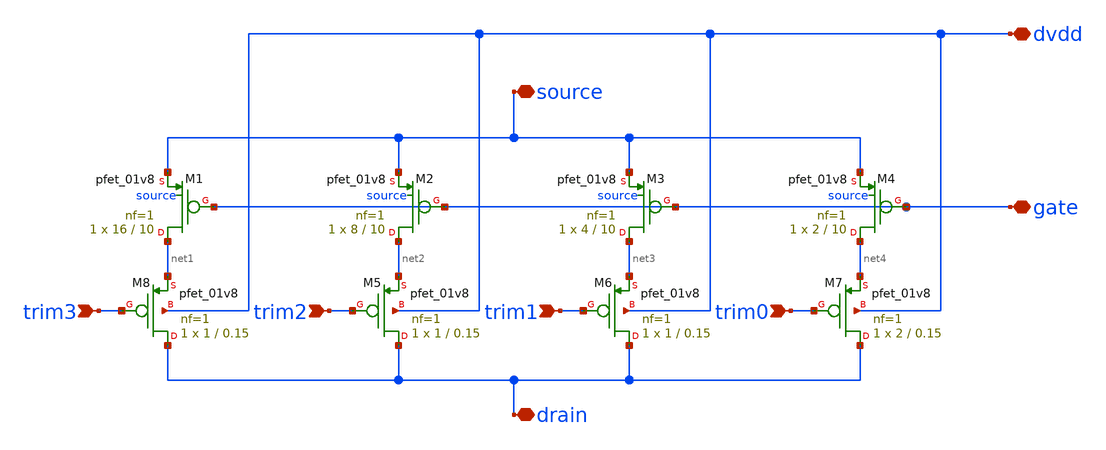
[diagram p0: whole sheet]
** sch_path: xschem/trim_pfet.sch
**.subckt trim_pfet trim0 trim1 trim2 trim3 dvdd drain source gate
*.ipin trim0
*.ipin trim1
*.ipin trim2
*.ipin trim3
*.iopin dvdd
*.iopin drain
*.iopin source
*.iopin gate
XM4 net4 gate source source sky130_fd_pr__pfet_01v8 L=10 W=2 nf=1 ad='int((nf+1)/2) * W/nf * 0.29' as='int((nf+2)/2) * W/nf * 0.29'
+ pd='2*int((nf+1)/2) * (W/nf + 0.29)' ps='2*int((nf+2)/2) * (W/nf + 0.29)' nrd='0.29 / W' nrs='0.29 / W'
+ sa=0 sb=0 sd=0 mult=1 m=1
XM3 net3 gate source source sky130_fd_pr__pfet_01v8 L=10 W=4 nf=1 ad='int((nf+1)/2) * W/nf * 0.29' as='int((nf+2)/2) * W/nf * 0.29'
+ pd='2*int((nf+1)/2) * (W/nf + 0.29)' ps='2*int((nf+2)/2) * (W/nf + 0.29)' nrd='0.29 / W' nrs='0.29 / W'
+ sa=0 sb=0 sd=0 mult=1 m=1
XM7 drain trim0 net4 dvdd sky130_fd_pr__pfet_01v8 L=0.15 W=2 nf=1 ad='int((nf+1)/2) * W/nf * 0.29' as='int((nf+2)/2) * W/nf * 0.29'
+ pd='2*int((nf+1)/2) * (W/nf + 0.29)' ps='2*int((nf+2)/2) * (W/nf + 0.29)' nrd='0.29 / W' nrs='0.29 / W'
+ sa=0 sb=0 sd=0 mult=1 m=1
XM6 drain trim1 net3 dvdd sky130_fd_pr__pfet_01v8 L=0.15 W=1 nf=1 ad='int((nf+1)/2) * W/nf * 0.29' as='int((nf+2)/2) * W/nf * 0.29'
+ pd='2*int((nf+1)/2) * (W/nf + 0.29)' ps='2*int((nf+2)/2) * (W/nf + 0.29)' nrd='0.29 / W' nrs='0.29 / W'
+ sa=0 sb=0 sd=0 mult=1 m=1
XM2 net2 gate source source sky130_fd_pr__pfet_01v8 L=10 W=8 nf=1 ad='int((nf+1)/2) * W/nf * 0.29' as='int((nf+2)/2) * W/nf * 0.29'
+ pd='2*int((nf+1)/2) * (W/nf + 0.29)' ps='2*int((nf+2)/2) * (W/nf + 0.29)' nrd='0.29 / W' nrs='0.29 / W'
+ sa=0 sb=0 sd=0 mult=1 m=1
XM5 drain trim2 net2 dvdd sky130_fd_pr__pfet_01v8 L=0.15 W=1 nf=1 ad='int((nf+1)/2) * W/nf * 0.29' as='int((nf+2)/2) * W/nf * 0.29'
+ pd='2*int((nf+1)/2) * (W/nf + 0.29)' ps='2*int((nf+2)/2) * (W/nf + 0.29)' nrd='0.29 / W' nrs='0.29 / W'
+ sa=0 sb=0 sd=0 mult=1 m=1
XM1 net1 gate source source sky130_fd_pr__pfet_01v8 L=10 W=16 nf=1 ad='int((nf+1)/2) * W/nf * 0.29' as='int((nf+2)/2) * W/nf * 0.29'
+ pd='2*int((nf+1)/2) * (W/nf + 0.29)' ps='2*int((nf+2)/2) * (W/nf + 0.29)' nrd='0.29 / W' nrs='0.29 / W'
+ sa=0 sb=0 sd=0 mult=1 m=1
XM8 drain trim3 net1 dvdd sky130_fd_pr__pfet_01v8 L=0.15 W=1 nf=1 ad='int((nf+1)/2) * W/nf * 0.29' as='int((nf+2)/2) * W/nf * 0.29'
+ pd='2*int((nf+1)/2) * (W/nf + 0.29)' ps='2*int((nf+2)/2) * (W/nf + 0.29)' nrd='0.29 / W' nrs='0.29 / W'
+ sa=0 sb=0 sd=0 mult=1 m=1
**.ends
.end
